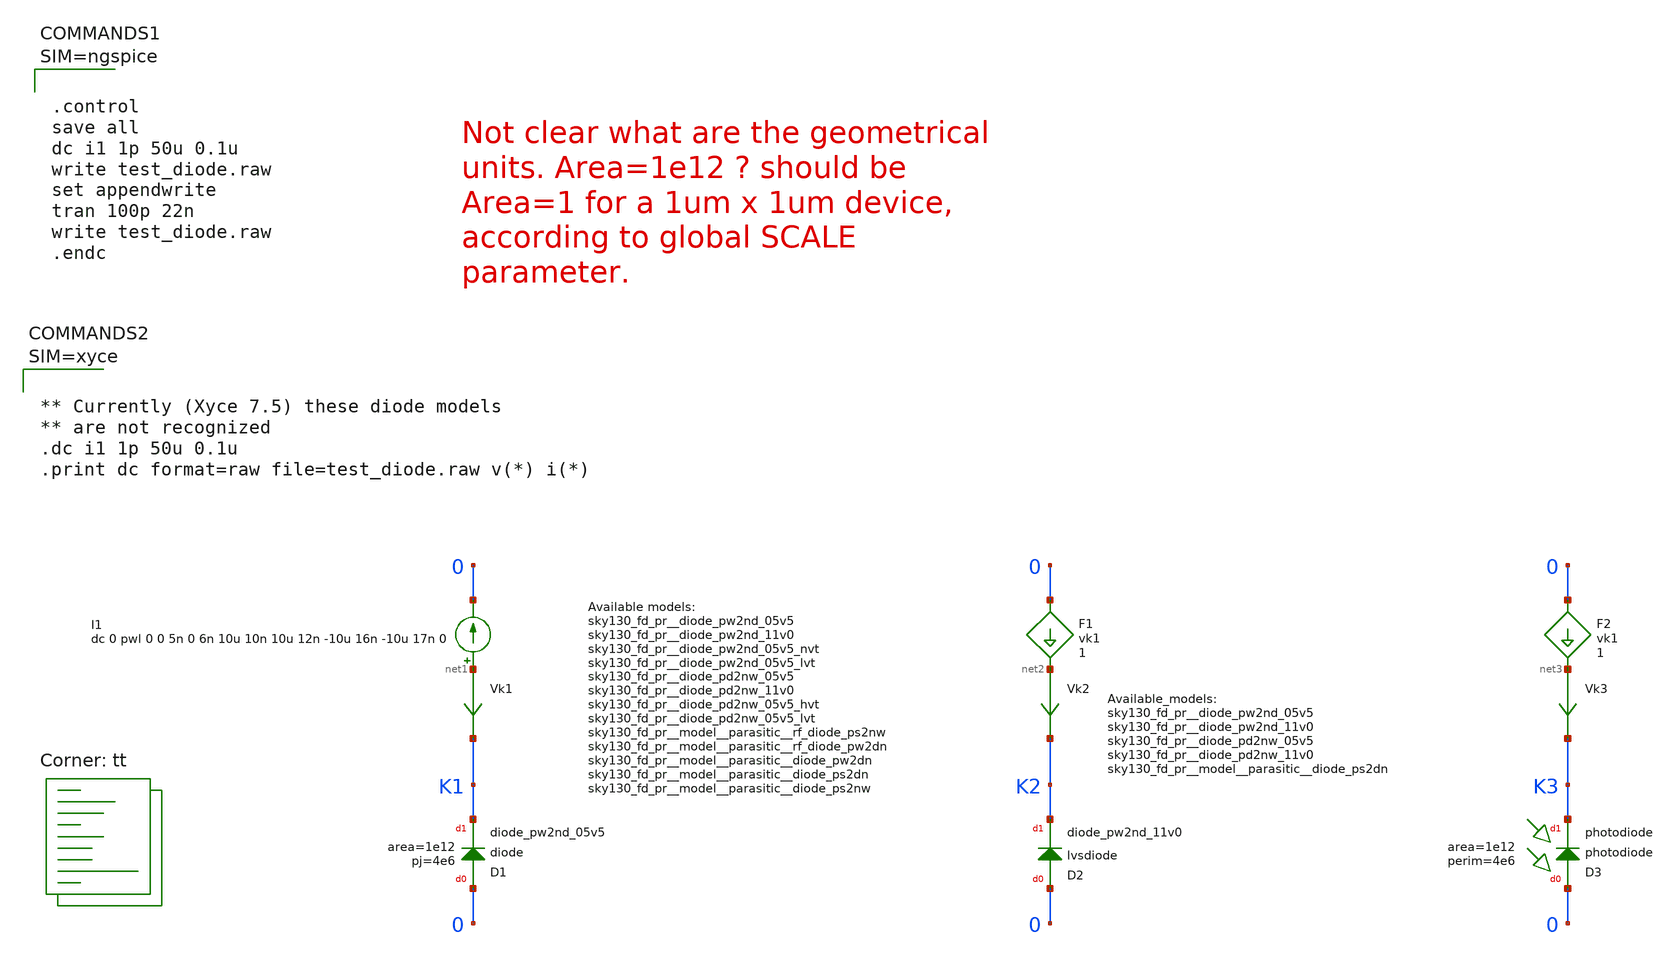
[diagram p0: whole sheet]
** sch_path: sky130A/xschem_libs/sky130_tests/test_diode/schematic/test_diode.sch
* Copyright 2021 Stefan Frederik Schippers
* Licensed under the Apache License, Version 2.0 (the "License");
* you may not use this file except in compliance with the License.
* You may obtain a copy of the License at
* https://www.apache.org/licenses/LICENSE-2.0
* Unless required by applicable law or agreed to in writing, software
* distributed under the License is distributed on an "AS IS" BASIS,
* WITHOUT WARRANTIES OR CONDITIONS OF ANY KIND, either express or implied.
* See the License for the specific language governing permissions and
* limitations under the License.
**.subckt test_diode
I1 net1 0 dc 0 pwl 0 0 5n 0 6n 10u 10n 10u 12n -10u 16n -10u 17n 0
XD1 0 K1 sky130_fd_pr__diode_pw2nd_05v5 area=1e12 pj=4e6
Vk2 net2 K2 0
.save i(vk2)
D2 0 K2 sky130_fd_pr__diode_pw2nd_11v0 area=1e12
F1 0 net2 vk1 1
Vk1 net1 K1 0
.save i(vk1)
XD3 0 K3 sky130_fd_pr__photodiode area=1e12 perim=4e6
Vk3 net3 K3 0
.save i(vk3)
F2 0 net3 vk1 1
**** begin user architecture code



.control
save all
dc i1 1p 50u 0.1u
write test_diode.raw
set appendwrite
tran 100p 22n
write test_diode.raw
.endc






.lib $::SKYWATER_MODELS/sky130.lib.spice tt
**** end user architecture code
**.ends
.end
